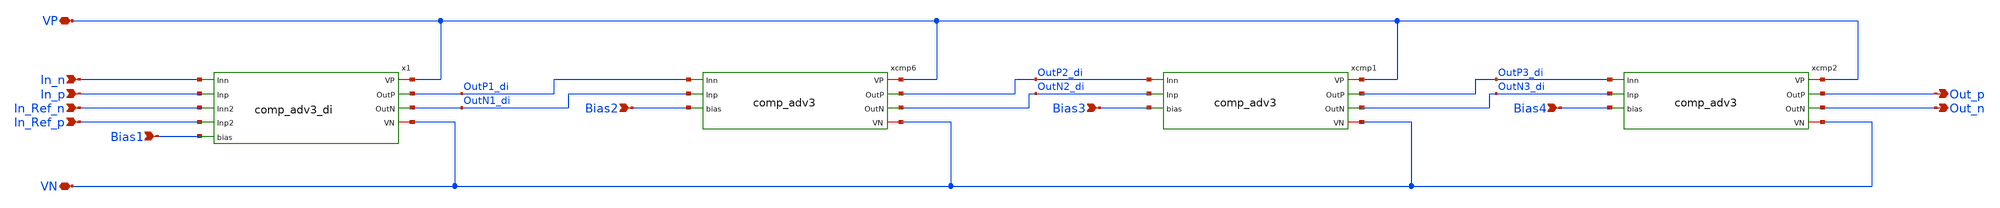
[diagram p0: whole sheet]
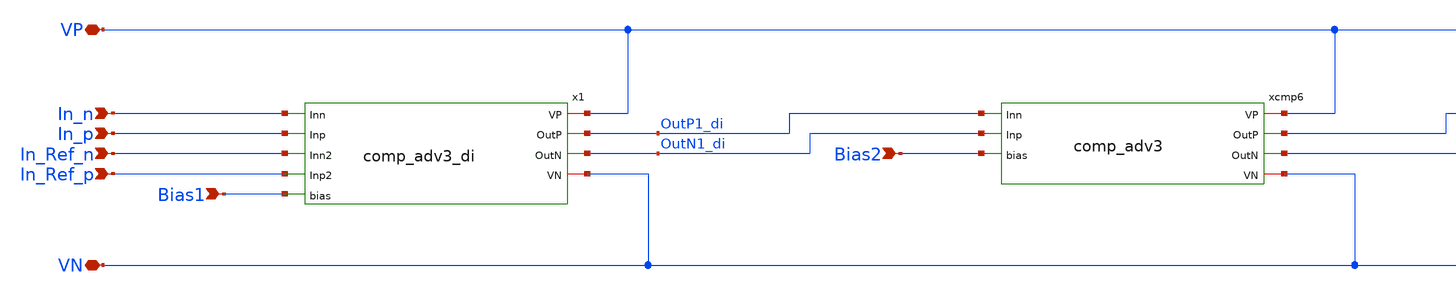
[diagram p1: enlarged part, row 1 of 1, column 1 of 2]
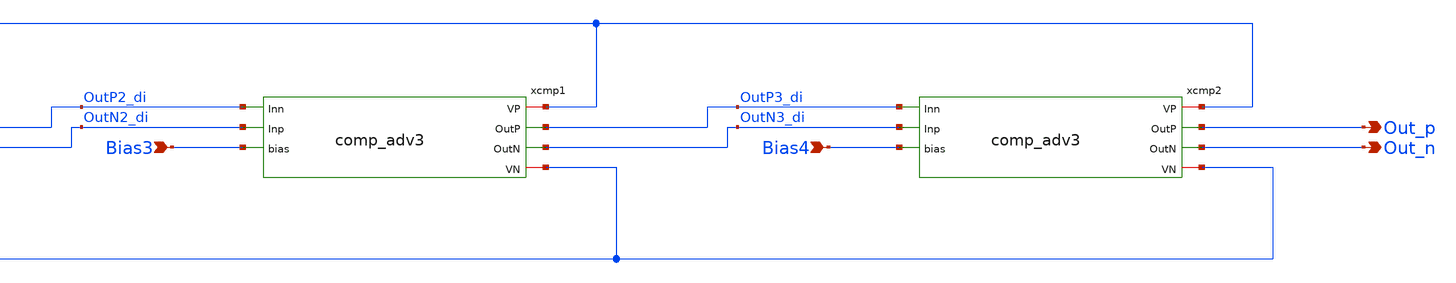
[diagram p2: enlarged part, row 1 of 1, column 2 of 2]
** sch_path: xschem/comp/comp_amp_di_40db_no_cmm.sch
**.subckt comp_amp_di_40db_no_cmm In_n VP Out_p In_p Bias1 Bias2 VN Out_n Bias3 Bias4 In_Ref_n
*+ In_Ref_p
*.ipin In_n
*.iopin VP
*.opin Out_p
*.ipin In_p
*.ipin Bias1
*.ipin Bias2
*.iopin VN
*.opin Out_n
*.ipin Bias3
*.ipin Bias4
*.ipin In_Ref_n
*.ipin In_Ref_p
xcmp6 VP OutP2_di OutN2_di OutP1_di OutN1_di Bias2 VN comp_adv3
xcmp1 VP OutP3_di OutN3_di OutP2_di OutN2_di Bias3 VN comp_adv3
xcmp2 VP Out_p Out_n OutP3_di OutN3_di Bias4 VN comp_adv3
x1 VP OutP1_di OutN1_di In_n In_p In_Ref_n In_Ref_p Bias1 VN comp_adv3_di
**.ends

* expanding   symbol:  comp/comp_adv3.sym # of pins=7
** sym_path: xschem/comp/comp_adv3.sym
** sch_path: xschem/comp/comp_adv3.sch
.subckt comp_adv3 VP OutP OutN Inn Inp bias VN
*.ipin Inp
*.ipin bias
*.ipin Inn
*.iopin VP
*.iopin VN
*.opin OutN
*.opin OutP
XM1 OutN Inp VIq VN sky130_fd_pr__nfet_01v8_lvt L=0.15 W=2 nf=1 ad='int((nf+1)/2) * W/nf * 0.29' as='int((nf+2)/2) * W/nf * 0.29'
+ pd='2*int((nf+1)/2) * (W/nf + 0.29)' ps='2*int((nf+2)/2) * (W/nf + 0.29)' nrd='0.29 / W' nrs='0.29 / W'
+ sa=0 sb=0 sd=0 mult=6 m=6
XM2 OutP Inn VIq VN sky130_fd_pr__nfet_01v8_lvt L=0.15 W=2 nf=1 ad='int((nf+1)/2) * W/nf * 0.29' as='int((nf+2)/2) * W/nf * 0.29'
+ pd='2*int((nf+1)/2) * (W/nf + 0.29)' ps='2*int((nf+2)/2) * (W/nf + 0.29)' nrd='0.29 / W' nrs='0.29 / W'
+ sa=0 sb=0 sd=0 mult=6 m=6
XM7 bias bias VN VN sky130_fd_pr__nfet_01v8_lvt L=0.3 W=2 nf=1 ad='int((nf+1)/2) * W/nf * 0.29' as='int((nf+2)/2) * W/nf * 0.29'
+ pd='2*int((nf+1)/2) * (W/nf + 0.29)' ps='2*int((nf+2)/2) * (W/nf + 0.29)' nrd='0.29 / W' nrs='0.29 / W'
+ sa=0 sb=0 sd=0 mult=1 m=1
XM9 VIq bias VN VN sky130_fd_pr__nfet_01v8_lvt L=0.3 W=2 nf=1 ad='int((nf+1)/2) * W/nf * 0.29' as='int((nf+2)/2) * W/nf * 0.29'
+ pd='2*int((nf+1)/2) * (W/nf + 0.29)' ps='2*int((nf+2)/2) * (W/nf + 0.29)' nrd='0.29 / W' nrs='0.29 / W'
+ sa=0 sb=0 sd=0 mult=10 m=10
XR1 OutN VP VN sky130_fd_pr__res_xhigh_po_2p85 L=1.5 mult=1 m=1
XR2 OutP VP VN sky130_fd_pr__res_xhigh_po_2p85 L=1.5 mult=1 m=1
XM3 bias VN VN VN sky130_fd_pr__nfet_01v8_lvt L=0.3 W=2 nf=1 ad='int((nf+1)/2) * W/nf * 0.29' as='int((nf+2)/2) * W/nf * 0.29'
+ pd='2*int((nf+1)/2) * (W/nf + 0.29)' ps='2*int((nf+2)/2) * (W/nf + 0.29)' nrd='0.29 / W' nrs='0.29 / W'
+ sa=0 sb=0 sd=0 mult=1 m=1
.ends


* expanding   symbol:  comp/comp_adv3_di.sym # of pins=9
** sym_path: xschem/comp/comp_adv3_di.sym
** sch_path: xschem/comp/comp_adv3_di.sch
.subckt comp_adv3_di VP OutP OutN Inn Inp Inn2 Inp2 bias VN
*.ipin Inp
*.ipin bias
*.ipin Inn
*.iopin VP
*.iopin VN
*.opin OutN
*.opin OutP
*.ipin Inn2
*.ipin Inp2
XM1 OutN Inp VIq VN sky130_fd_pr__nfet_01v8_lvt L=0.15 W=2 nf=1 ad='int((nf+1)/2) * W/nf * 0.29' as='int((nf+2)/2) * W/nf * 0.29'
+ pd='2*int((nf+1)/2) * (W/nf + 0.29)' ps='2*int((nf+2)/2) * (W/nf + 0.29)' nrd='0.29 / W' nrs='0.29 / W'
+ sa=0 sb=0 sd=0 mult=6 m=6
XM2 OutP Inn VIq VN sky130_fd_pr__nfet_01v8_lvt L=0.15 W=2 nf=1 ad='int((nf+1)/2) * W/nf * 0.29' as='int((nf+2)/2) * W/nf * 0.29'
+ pd='2*int((nf+1)/2) * (W/nf + 0.29)' ps='2*int((nf+2)/2) * (W/nf + 0.29)' nrd='0.29 / W' nrs='0.29 / W'
+ sa=0 sb=0 sd=0 mult=6 m=6
XM7 bias bias VN VN sky130_fd_pr__nfet_01v8_lvt L=0.3 W=2 nf=1 ad='int((nf+1)/2) * W/nf * 0.29' as='int((nf+2)/2) * W/nf * 0.29'
+ pd='2*int((nf+1)/2) * (W/nf + 0.29)' ps='2*int((nf+2)/2) * (W/nf + 0.29)' nrd='0.29 / W' nrs='0.29 / W'
+ sa=0 sb=0 sd=0 mult=1 m=1
XM9 VIq bias VN VN sky130_fd_pr__nfet_01v8_lvt L=0.3 W=2 nf=1 ad='int((nf+1)/2) * W/nf * 0.29' as='int((nf+2)/2) * W/nf * 0.29'
+ pd='2*int((nf+1)/2) * (W/nf + 0.29)' ps='2*int((nf+2)/2) * (W/nf + 0.29)' nrd='0.29 / W' nrs='0.29 / W'
+ sa=0 sb=0 sd=0 mult=10 m=10
XR1 OutN VP VN sky130_fd_pr__res_xhigh_po_2p85 L=1 mult=1 m=1
XR2 OutP VP VN sky130_fd_pr__res_xhigh_po_2p85 L=1 mult=1 m=1
XM3 OutN Inp2 VN VN sky130_fd_pr__nfet_01v8_lvt L=0.15 W=2 nf=1 ad='int((nf+1)/2) * W/nf * 0.29' as='int((nf+2)/2) * W/nf * 0.29'
+ pd='2*int((nf+1)/2) * (W/nf + 0.29)' ps='2*int((nf+2)/2) * (W/nf + 0.29)' nrd='0.29 / W' nrs='0.29 / W'
+ sa=0 sb=0 sd=0 mult=1 m=1
XM4 OutP Inn2 VN VN sky130_fd_pr__nfet_01v8_lvt L=0.15 W=2 nf=1 ad='int((nf+1)/2) * W/nf * 0.29' as='int((nf+2)/2) * W/nf * 0.29'
+ pd='2*int((nf+1)/2) * (W/nf + 0.29)' ps='2*int((nf+2)/2) * (W/nf + 0.29)' nrd='0.29 / W' nrs='0.29 / W'
+ sa=0 sb=0 sd=0 mult=1 m=1
XM5 Inn2 Inn2 VN VN sky130_fd_pr__nfet_01v8_lvt L=0.15 W=2 nf=1 ad='int((nf+1)/2) * W/nf * 0.29' as='int((nf+2)/2) * W/nf * 0.29'
+ pd='2*int((nf+1)/2) * (W/nf + 0.29)' ps='2*int((nf+2)/2) * (W/nf + 0.29)' nrd='0.29 / W' nrs='0.29 / W'
+ sa=0 sb=0 sd=0 mult=1 m=1
XM6 Inp2 Inp2 VN VN sky130_fd_pr__nfet_01v8_lvt L=0.15 W=2 nf=1 ad='int((nf+1)/2) * W/nf * 0.29' as='int((nf+2)/2) * W/nf * 0.29'
+ pd='2*int((nf+1)/2) * (W/nf + 0.29)' ps='2*int((nf+2)/2) * (W/nf + 0.29)' nrd='0.29 / W' nrs='0.29 / W'
+ sa=0 sb=0 sd=0 mult=1 m=1
XM8 Inp2 VN VN VN sky130_fd_pr__nfet_01v8_lvt L=0.15 W=2 nf=1 ad='int((nf+1)/2) * W/nf * 0.29' as='int((nf+2)/2) * W/nf * 0.29'
+ pd='2*int((nf+1)/2) * (W/nf + 0.29)' ps='2*int((nf+2)/2) * (W/nf + 0.29)' nrd='0.29 / W' nrs='0.29 / W'
+ sa=0 sb=0 sd=0 mult=1 m=1
XM10 Inn2 VN VN VN sky130_fd_pr__nfet_01v8_lvt L=0.15 W=2 nf=1 ad='int((nf+1)/2) * W/nf * 0.29' as='int((nf+2)/2) * W/nf * 0.29'
+ pd='2*int((nf+1)/2) * (W/nf + 0.29)' ps='2*int((nf+2)/2) * (W/nf + 0.29)' nrd='0.29 / W' nrs='0.29 / W'
+ sa=0 sb=0 sd=0 mult=1 m=1
XM11 bias VN VN VN sky130_fd_pr__nfet_01v8_lvt L=0.3 W=2 nf=1 ad='int((nf+1)/2) * W/nf * 0.29' as='int((nf+2)/2) * W/nf * 0.29'
+ pd='2*int((nf+1)/2) * (W/nf + 0.29)' ps='2*int((nf+2)/2) * (W/nf + 0.29)' nrd='0.29 / W' nrs='0.29 / W'
+ sa=0 sb=0 sd=0 mult=1 m=1
.ends

.end
